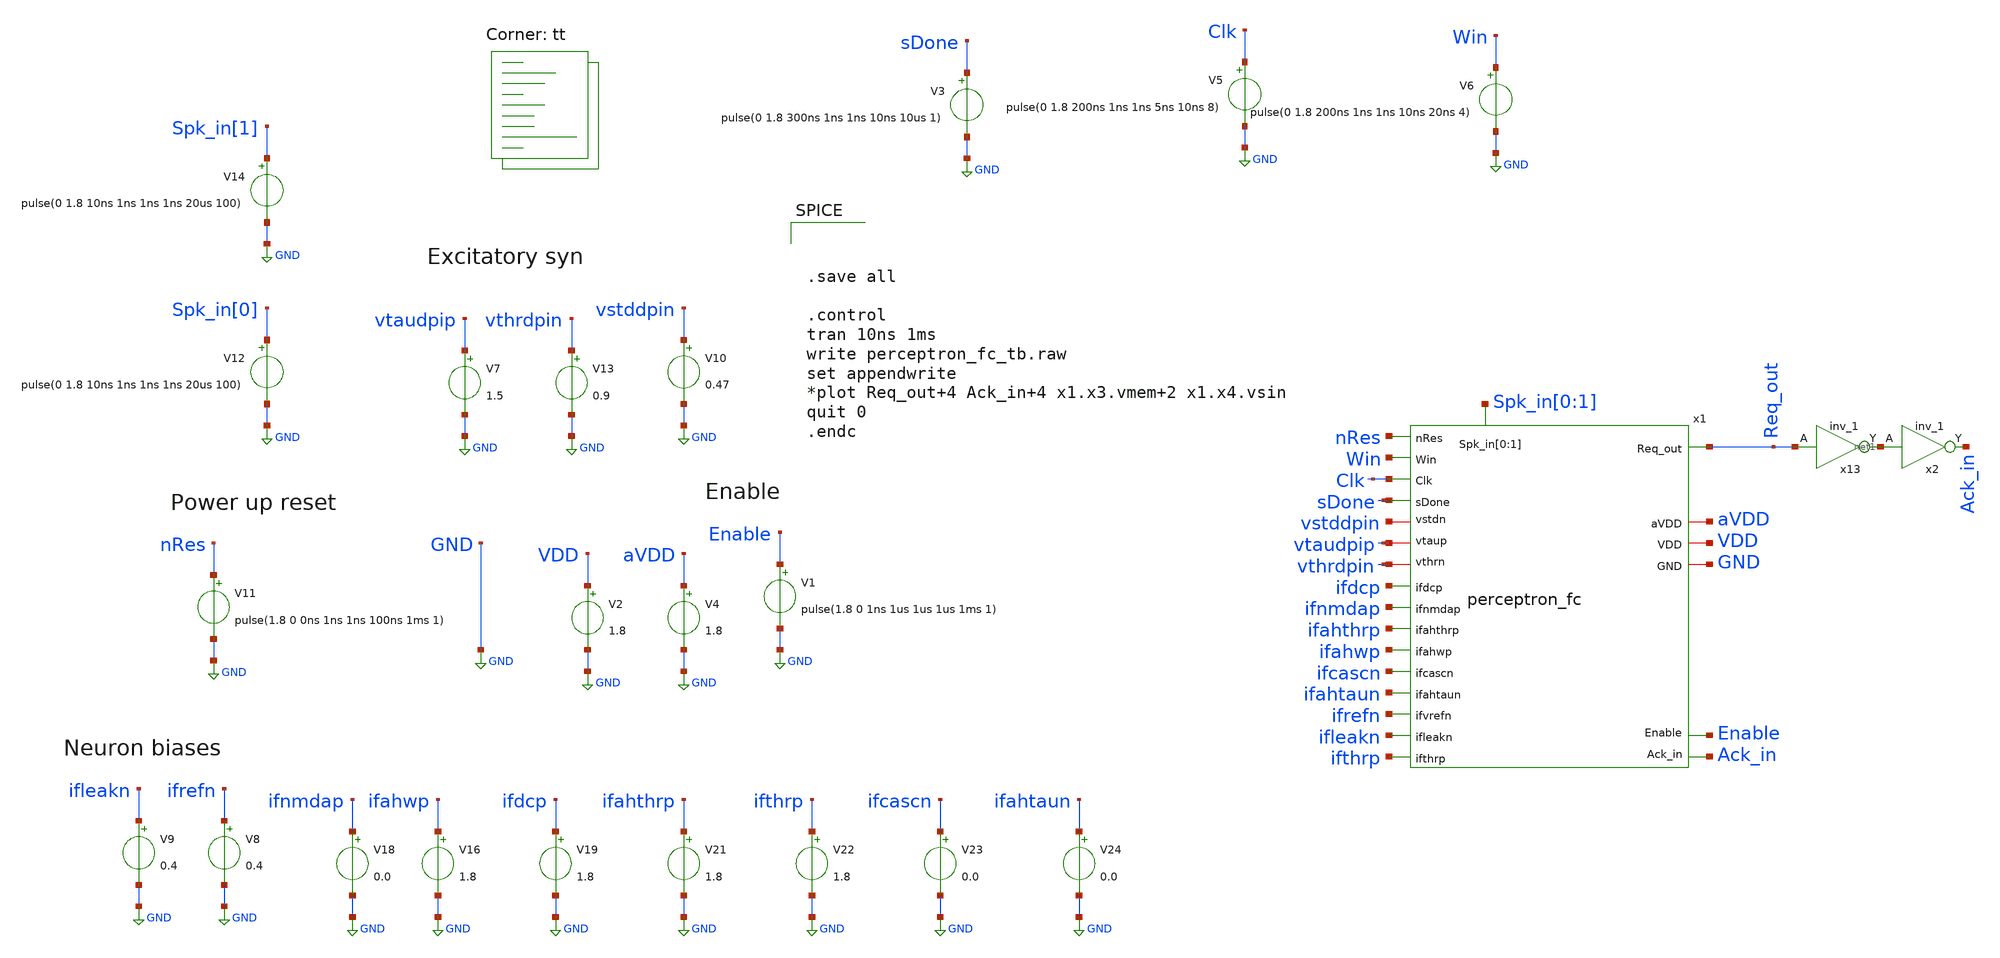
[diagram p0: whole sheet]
** sch_path: design/xschem/perceptron_fc_tb.sch
**.subckt perceptron_fc_tb
V8 ifrefn GND 0.4
V9 ifleakn GND 0.4
V16 ifahwp GND 1.8
V18 ifnmdap GND 0.0
V19 ifdcp GND 1.8
V21 ifahthrp GND 1.8
V22 ifthrp GND 1.8
V23 ifcascn GND 0.0
V24 ifahtaun GND 0.0
V2 VDD GND 1.8
V7 vtaudpip GND 1.5
V13 vthrdpin GND 0.9
V10 vstddpin GND 0.47
V12 Spk_in[0] GND pulse(0 1.8 10ns 1ns 1ns 1ns 20us 100)
V4 aVDD GND 1.8
V11 nRes GND pulse(1.8 0 0ns 1ns 1ns 100ns 1ms 1)
x13 Req_out 0 0 VDD VDD net1 sky130_fd_sc_hd__inv_1
x2 net1 0 0 VDD VDD Ack_in sky130_fd_sc_hd__inv_1
V1 Enable GND pulse(1.8 0 1ns 1us 1us 1us 1ms 1)
V3 sDone GND pulse(0 1.8 300ns 1ns 1ns 10ns 10us 1)
V5 Clk GND pulse(0 1.8 200ns 1ns 1ns 5ns 10ns 8)
V6 Win GND pulse(0 1.8 200ns 1ns 1ns 10ns 20ns 4)
x1 GND ifdcp VDD vthrdpin Win Req_out aVDD ifnmdap vtaudpip Clk ifthrp nRes vstddpin ifleakn sDone
+ Ack_in ifahthrp Enable ifahwp ifcascn Spk_in[0] Spk_in[1] ifahtaun ifrefn perceptron_fc
V14 Spk_in[1] GND pulse(0 1.8 10ns 1ns 1ns 1ns 20us 100)
**** begin user architecture code


* Standard cell simulation files
.include $::SKYWATER_STDCELLS/sky130_fd_sc_hd.spice

.lib $::SKYWATER_MODELS/sky130.lib.spice tt



.save all

.control
tran 10ns 1ms
write perceptron_fc_tb.raw
set appendwrite
*plot Req_out+4 Ack_in+4 x1.x3.vmem+2 x1.x4.vsin
quit 0
.endc


**** end user architecture code
**.ends

* expanding   symbol:  perceptron_fc.sym # of pins=23
** sym_path: design/xschem/perceptron_fc.sym
** sch_path: design/xschem/perceptron_fc.sch
.subckt perceptron_fc GND ifdcp VDD vthrn Win Req_out aVDD ifnmdap vtaup Clk ifthrp nRes vstdn
+ ifleakn sDone Ack_in ifahthrp Enable ifahwp ifcascn Spk_in[0] Spk_in[1] ifahtaun ifvrefn
*.iopin GND
*.iopin VDD
*.iopin aVDD
*.ipin Enable
*.ipin Clk
*.ipin nRes
*.ipin sDone
*.ipin Spk_in[0],Spk_in[1]
*.ipin Ack_in
*.opin Req_out
*.ipin ifdcp
*.ipin ifnmdap
*.ipin ifthrp
*.ipin ifleakn
*.ipin ifahthrp
*.ipin ifahwp
*.ipin ifcascn
*.ipin ifahtaun
*.ipin ifvrefn
*.iopin vthrn
*.iopin vtaup
*.iopin vstdn
*.ipin Win
x3 nreq_neu0 sinp0 nack_cel0 ifnmdap ifahwp ifdcp net2 ifahthrp ifthrp ifcascn ifleakn ifvrefn
+ ifahtaun GND aVDD neuron_analog_fc
x14 nRes Req_out Ack_in ack_cel0 VDD GND c_element_rj
x4 vtaup STOT vthrn Spk_in[0] vstdn GND VDD D[0] D[1] D[2] D[3] dpi_syn_exc_4bit_fc
x5 Win D[0] D[1] D[2] D[3] Dout1 Clk nRes sDone GND VDD dflip_flop_chain_4_fc
x13 ack_cel0 GND GND VDD VDD nack_cel0 sky130_fd_sc_hd__inv_1
x1 Enable sinp0 STOT GND aVDD tranmission_gate_fc
x2 Enable Req_out net1 GND aVDD tranmission_gate_fc
x7 Dout1 D[4] D[5] D[6] D[7] net3 Clk nRes sDone GND VDD dflip_flop_chain_4_fc
x6 vtaup STOT vthrn Spk_in[1] vstdn GND VDD D[4] D[5] D[6] D[7] dpi_syn_exc_4bit_fc
x9 nreq_neu0 net1 VDD GND schmitt_trigger
.ends


* expanding   symbol:  neuron_analog_fc.sym # of pins=15
** sym_path: design/xschem/neuron_analog_fc.sym
** sch_path: design/xschem/neuron_analog_fc.sch
.subckt neuron_analog_fc nreq sinp nack ifahwp ifnmdap ifahthrp vmem ifdcp ifthrp ifcascn vleakn
+ vrefn ifahtaun GND VDD
*.ipin vleakn
*.iopin GND
*.iopin VDD
*.opin nreq
*.ipin vrefn
*.ipin nack
*.ipin ifdcp
*.ipin ifthrp
*.ipin ifnmdap
*.ipin ifahwp
*.ipin ifahthrp
*.ipin ifahtaun
*.ipin ifcascn
*.iopin vmem
*.iopin sinp
XC1 GND vmem sky130_fd_pr__cap_mim_m3_1 W=11 L=11 MF=1 m=1
XM8 net4 vrefn GND GND sky130_fd_pr__nfet_01v8 L=0.25 W=0.8 nf=1 ad='int((nf+1)/2) * W/nf * 0.29' as='int((nf+2)/2) * W/nf * 0.29'
+ pd='2*int((nf+1)/2) * (W/nf + 0.29)' ps='2*int((nf+2)/2) * (W/nf + 0.29)' nrd='0.29 / W' nrs='0.29 / W'
+ sa=0 sb=0 sd=0 mult=1 m=1
XM9 net5 nack VDD VDD sky130_fd_pr__pfet_01v8 L=0.2 W=1.2 nf=1 ad='int((nf+1)/2) * W/nf * 0.29' as='int((nf+2)/2) * W/nf * 0.29'
+ pd='2*int((nf+1)/2) * (W/nf + 0.29)' ps='2*int((nf+2)/2) * (W/nf + 0.29)' nrd='0.29 / W' nrs='0.29 / W'
+ sa=0 sb=0 sd=0 mult=1 m=1
XC2 GND net3 sky130_fd_pr__cap_mim_m3_1 W=4 L=2 MF=1 m=1
XM21 vmem net3 GND GND sky130_fd_pr__nfet_01v8 L=0.25 W=1 nf=1 ad='int((nf+1)/2) * W/nf * 0.29' as='int((nf+2)/2) * W/nf * 0.29'
+ pd='2*int((nf+1)/2) * (W/nf + 0.29)' ps='2*int((nf+2)/2) * (W/nf + 0.29)' nrd='0.29 / W' nrs='0.29 / W'
+ sa=0 sb=0 sd=0 mult=1 m=1
XM15 net12 ifnmdap sinp VDD sky130_fd_pr__pfet_01v8 L=0.15 W=1 nf=1 ad='int((nf+1)/2) * W/nf * 0.29'
+ as='int((nf+2)/2) * W/nf * 0.29' pd='2*int((nf+1)/2) * (W/nf + 0.29)' ps='2*int((nf+2)/2) * (W/nf + 0.29)'
+ nrd='0.29 / W' nrs='0.29 / W' sa=0 sb=0 sd=0 mult=1 m=1
XC3 GND net8 sky130_fd_pr__cap_mim_m3_1 W=5 L=5 MF=1 m=1
XM12 GND vmem sinp VDD sky130_fd_pr__pfet_01v8 L=0.15 W=1 nf=1 ad='int((nf+1)/2) * W/nf * 0.29' as='int((nf+2)/2) * W/nf * 0.29'
+ pd='2*int((nf+1)/2) * (W/nf + 0.29)' ps='2*int((nf+2)/2) * (W/nf + 0.29)' nrd='0.29 / W' nrs='0.29 / W'
+ sa=0 sb=0 sd=0 mult=1 m=1
XM11 GND ifthrp net6 VDD sky130_fd_pr__pfet_01v8 L=0.15 W=1 nf=1 ad='int((nf+1)/2) * W/nf * 0.29' as='int((nf+2)/2) * W/nf * 0.29'
+ pd='2*int((nf+1)/2) * (W/nf + 0.29)' ps='2*int((nf+2)/2) * (W/nf + 0.29)' nrd='0.29 / W' nrs='0.29 / W'
+ sa=0 sb=0 sd=0 mult=1 m=1
XM16 net7 nack VDD VDD sky130_fd_pr__pfet_01v8 L=0.15 W=1 nf=1 ad='int((nf+1)/2) * W/nf * 0.29' as='int((nf+2)/2) * W/nf * 0.29'
+ pd='2*int((nf+1)/2) * (W/nf + 0.29)' ps='2*int((nf+2)/2) * (W/nf + 0.29)' nrd='0.29 / W' nrs='0.29 / W'
+ sa=0 sb=0 sd=0 mult=1 m=1
XM17 net9 ifahwp net7 VDD sky130_fd_pr__pfet_01v8 L=0.15 W=1 nf=1 ad='int((nf+1)/2) * W/nf * 0.29' as='int((nf+2)/2) * W/nf * 0.29'
+ pd='2*int((nf+1)/2) * (W/nf + 0.29)' ps='2*int((nf+2)/2) * (W/nf + 0.29)' nrd='0.29 / W' nrs='0.29 / W'
+ sa=0 sb=0 sd=0 mult=1 m=1
XM18 GND ifahthrp net9 VDD sky130_fd_pr__pfet_01v8 L=0.15 W=1 nf=1 ad='int((nf+1)/2) * W/nf * 0.29' as='int((nf+2)/2) * W/nf * 0.29'
+ pd='2*int((nf+1)/2) * (W/nf + 0.29)' ps='2*int((nf+2)/2) * (W/nf + 0.29)' nrd='0.29 / W' nrs='0.29 / W'
+ sa=0 sb=0 sd=0 mult=1 m=1
XM19 net8 net8 net9 VDD sky130_fd_pr__pfet_01v8 L=0.15 W=1 nf=1 ad='int((nf+1)/2) * W/nf * 0.29' as='int((nf+2)/2) * W/nf * 0.29'
+ pd='2*int((nf+1)/2) * (W/nf + 0.29)' ps='2*int((nf+2)/2) * (W/nf + 0.29)' nrd='0.29 / W' nrs='0.29 / W'
+ sa=0 sb=0 sd=0 mult=1 m=1
XM1 net11 ifdcp VDD VDD sky130_fd_pr__pfet_01v8 L=0.3 W=1 nf=1 ad='int((nf+1)/2) * W/nf * 0.29' as='int((nf+2)/2) * W/nf * 0.29'
+ pd='2*int((nf+1)/2) * (W/nf + 0.29)' ps='2*int((nf+2)/2) * (W/nf + 0.29)' nrd='0.29 / W' nrs='0.29 / W'
+ sa=0 sb=0 sd=0 mult=1 m=1
XM5 net2 nreq VDD VDD sky130_fd_pr__pfet_01v8 L=0.15 W=1 nf=1 ad='int((nf+1)/2) * W/nf * 0.29' as='int((nf+2)/2) * W/nf * 0.29'
+ pd='2*int((nf+1)/2) * (W/nf + 0.29)' ps='2*int((nf+2)/2) * (W/nf + 0.29)' nrd='0.29 / W' nrs='0.29 / W'
+ sa=0 sb=0 sd=0 mult=1 m=1
XM6 nreq vmem net2 VDD sky130_fd_pr__pfet_01v8 L=0.15 W=1 nf=1 ad='int((nf+1)/2) * W/nf * 0.29' as='int((nf+2)/2) * W/nf * 0.29'
+ pd='2*int((nf+1)/2) * (W/nf + 0.29)' ps='2*int((nf+2)/2) * (W/nf + 0.29)' nrd='0.29 / W' nrs='0.29 / W'
+ sa=0 sb=0 sd=0 mult=1 m=1
XM10 net3 nreq net5 VDD sky130_fd_pr__pfet_01v8 L=0.15 W=1 nf=1 ad='int((nf+1)/2) * W/nf * 0.29' as='int((nf+2)/2) * W/nf * 0.29'
+ pd='2*int((nf+1)/2) * (W/nf + 0.29)' ps='2*int((nf+2)/2) * (W/nf + 0.29)' nrd='0.29 / W' nrs='0.29 / W'
+ sa=0 sb=0 sd=0 mult=1 m=1
XM2 nreq vmem net1 GND sky130_fd_pr__nfet_01v8 L=0.15 W=0.65 nf=1 ad='int((nf+1)/2) * W/nf * 0.29' as='int((nf+2)/2) * W/nf * 0.29'
+ pd='2*int((nf+1)/2) * (W/nf + 0.29)' ps='2*int((nf+2)/2) * (W/nf + 0.29)' nrd='0.29 / W' nrs='0.29 / W'
+ sa=0 sb=0 sd=0 mult=1 m=1
XM3 net1 net1 GND GND sky130_fd_pr__nfet_01v8 L=0.15 W=0.65 nf=1 ad='int((nf+1)/2) * W/nf * 0.29' as='int((nf+2)/2) * W/nf * 0.29'
+ pd='2*int((nf+1)/2) * (W/nf + 0.29)' ps='2*int((nf+2)/2) * (W/nf + 0.29)' nrd='0.29 / W' nrs='0.29 / W'
+ sa=0 sb=0 sd=0 mult=1 m=1
XM7 net3 nreq net4 GND sky130_fd_pr__nfet_01v8 L=0.15 W=0.65 nf=1 ad='int((nf+1)/2) * W/nf * 0.29' as='int((nf+2)/2) * W/nf * 0.29'
+ pd='2*int((nf+1)/2) * (W/nf + 0.29)' ps='2*int((nf+2)/2) * (W/nf + 0.29)' nrd='0.29 / W' nrs='0.29 / W'
+ sa=0 sb=0 sd=0 mult=1 m=1
XM14 vmem vleakn net13 GND sky130_fd_pr__nfet_01v8 L=0.15 W=0.65 nf=1 ad='int((nf+1)/2) * W/nf * 0.29'
+ as='int((nf+2)/2) * W/nf * 0.29' pd='2*int((nf+1)/2) * (W/nf + 0.29)' ps='2*int((nf+2)/2) * (W/nf + 0.29)'
+ nrd='0.29 / W' nrs='0.29 / W' sa=0 sb=0 sd=0 mult=1 m=1
XM4 vmem nreq VDD VDD sky130_fd_pr__pfet_01v8 L=0.15 W=1 nf=1 ad='int((nf+1)/2) * W/nf * 0.29' as='int((nf+2)/2) * W/nf * 0.29'
+ pd='2*int((nf+1)/2) * (W/nf + 0.29)' ps='2*int((nf+2)/2) * (W/nf + 0.29)' nrd='0.29 / W' nrs='0.29 / W'
+ sa=0 sb=0 sd=0 mult=1 m=1
XM24 vmem vmem net6 VDD sky130_fd_pr__pfet_01v8 L=0.15 W=1 nf=1 ad='int((nf+1)/2) * W/nf * 0.29' as='int((nf+2)/2) * W/nf * 0.29'
+ pd='2*int((nf+1)/2) * (W/nf + 0.29)' ps='2*int((nf+2)/2) * (W/nf + 0.29)' nrd='0.29 / W' nrs='0.29 / W'
+ sa=0 sb=0 sd=0 mult=1 m=1
Vmeas net11 net6 0
.save i(vmeas)
Vmeas1 net13 GND 0
.save i(vmeas1)
XM13 net6 ifcascn net10 GND sky130_fd_pr__nfet_01v8 L=0.15 W=0.65 nf=1 ad='int((nf+1)/2) * W/nf * 0.29'
+ as='int((nf+2)/2) * W/nf * 0.29' pd='2*int((nf+1)/2) * (W/nf + 0.29)' ps='2*int((nf+2)/2) * (W/nf + 0.29)'
+ nrd='0.29 / W' nrs='0.29 / W' sa=0 sb=0 sd=0 mult=1 m=1
XM20 net10 net8 GND GND sky130_fd_pr__nfet_01v8 L=0.15 W=0.65 nf=1 ad='int((nf+1)/2) * W/nf * 0.29' as='int((nf+2)/2) * W/nf * 0.29'
+ pd='2*int((nf+1)/2) * (W/nf + 0.29)' ps='2*int((nf+2)/2) * (W/nf + 0.29)' nrd='0.29 / W' nrs='0.29 / W'
+ sa=0 sb=0 sd=0 mult=1 m=1
XM22 net8 ifahtaun GND GND sky130_fd_pr__nfet_01v8 L=0.15 W=0.65 nf=1 ad='int((nf+1)/2) * W/nf * 0.29'
+ as='int((nf+2)/2) * W/nf * 0.29' pd='2*int((nf+1)/2) * (W/nf + 0.29)' ps='2*int((nf+2)/2) * (W/nf + 0.29)'
+ nrd='0.29 / W' nrs='0.29 / W' sa=0 sb=0 sd=0 mult=1 m=1
.ends


* expanding   symbol:  c_element_rj.sym # of pins=6
** sym_path: design/xschem/c_element_rj.sym
** sch_path: design/xschem/c_element_rj.sch
.subckt c_element_rj nrst a b c dVDD dGND
*.iopin dGND
*.iopin dVDD
*.opin c
*.ipin b
*.ipin a
*.ipin nrst
XM14 c net6 dVDD dVDD sky130_fd_pr__pfet_01v8 L=0.15 W=1 nf=1 ad='int((nf+1)/2) * W/nf * 0.29' as='int((nf+2)/2) * W/nf * 0.29'
+ pd='2*int((nf+1)/2) * (W/nf + 0.29)' ps='2*int((nf+2)/2) * (W/nf + 0.29)' nrd='0.29 / W' nrs='0.29 / W'
+ sa=0 sb=0 sd=0 mult=1 m=1
XM5 net6 nrst dVDD dVDD sky130_fd_pr__pfet_01v8 L=0.15 W=1 nf=1 ad='int((nf+1)/2) * W/nf * 0.29' as='int((nf+2)/2) * W/nf * 0.29'
+ pd='2*int((nf+1)/2) * (W/nf + 0.29)' ps='2*int((nf+2)/2) * (W/nf + 0.29)' nrd='0.29 / W' nrs='0.29 / W'
+ sa=0 sb=0 sd=0 mult=1 m=1
XM6 net5 b dVDD dVDD sky130_fd_pr__pfet_01v8 L=0.15 W=1 nf=1 ad='int((nf+1)/2) * W/nf * 0.29' as='int((nf+2)/2) * W/nf * 0.29'
+ pd='2*int((nf+1)/2) * (W/nf + 0.29)' ps='2*int((nf+2)/2) * (W/nf + 0.29)' nrd='0.29 / W' nrs='0.29 / W'
+ sa=0 sb=0 sd=0 mult=1 m=1
XM4 net4 a dVDD dVDD sky130_fd_pr__pfet_01v8 L=0.15 W=1 nf=1 ad='int((nf+1)/2) * W/nf * 0.29' as='int((nf+2)/2) * W/nf * 0.29'
+ pd='2*int((nf+1)/2) * (W/nf + 0.29)' ps='2*int((nf+2)/2) * (W/nf + 0.29)' nrd='0.29 / W' nrs='0.29 / W'
+ sa=0 sb=0 sd=0 mult=1 m=1
XM7 net3 b net4 dVDD sky130_fd_pr__pfet_01v8 L=0.15 W=1 nf=1 ad='int((nf+1)/2) * W/nf * 0.29' as='int((nf+2)/2) * W/nf * 0.29'
+ pd='2*int((nf+1)/2) * (W/nf + 0.29)' ps='2*int((nf+2)/2) * (W/nf + 0.29)' nrd='0.29 / W' nrs='0.29 / W'
+ sa=0 sb=0 sd=0 mult=1 m=1
XM8 net3 a net5 dVDD sky130_fd_pr__pfet_01v8 L=0.15 W=1 nf=1 ad='int((nf+1)/2) * W/nf * 0.29' as='int((nf+2)/2) * W/nf * 0.29'
+ pd='2*int((nf+1)/2) * (W/nf + 0.29)' ps='2*int((nf+2)/2) * (W/nf + 0.29)' nrd='0.29 / W' nrs='0.29 / W'
+ sa=0 sb=0 sd=0 mult=1 m=1
XM10 net5 c net4 dVDD sky130_fd_pr__pfet_01v8 L=0.15 W=1 nf=1 ad='int((nf+1)/2) * W/nf * 0.29' as='int((nf+2)/2) * W/nf * 0.29'
+ pd='2*int((nf+1)/2) * (W/nf + 0.29)' ps='2*int((nf+2)/2) * (W/nf + 0.29)' nrd='0.29 / W' nrs='0.29 / W'
+ sa=0 sb=0 sd=0 mult=1 m=1
XM12 c net6 dGND dGND sky130_fd_pr__nfet_01v8 L=0.15 W=0.65 nf=1 ad='int((nf+1)/2) * W/nf * 0.29' as='int((nf+2)/2) * W/nf * 0.29'
+ pd='2*int((nf+1)/2) * (W/nf + 0.29)' ps='2*int((nf+2)/2) * (W/nf + 0.29)' nrd='0.29 / W' nrs='0.29 / W'
+ sa=0 sb=0 sd=0 mult=1 m=1
XM1 net3 nrst net6 dGND sky130_fd_pr__nfet_01v8 L=0.15 W=0.65 nf=1 ad='int((nf+1)/2) * W/nf * 0.29' as='int((nf+2)/2) * W/nf * 0.29'
+ pd='2*int((nf+1)/2) * (W/nf + 0.29)' ps='2*int((nf+2)/2) * (W/nf + 0.29)' nrd='0.29 / W' nrs='0.29 / W'
+ sa=0 sb=0 sd=0 mult=1 m=1
XM2 net3 b net1 dGND sky130_fd_pr__nfet_01v8 L=0.15 W=0.65 nf=1 ad='int((nf+1)/2) * W/nf * 0.29' as='int((nf+2)/2) * W/nf * 0.29'
+ pd='2*int((nf+1)/2) * (W/nf + 0.29)' ps='2*int((nf+2)/2) * (W/nf + 0.29)' nrd='0.29 / W' nrs='0.29 / W'
+ sa=0 sb=0 sd=0 mult=1 m=1
XM3 net3 a net2 dGND sky130_fd_pr__nfet_01v8 L=0.15 W=0.65 nf=1 ad='int((nf+1)/2) * W/nf * 0.29' as='int((nf+2)/2) * W/nf * 0.29'
+ pd='2*int((nf+1)/2) * (W/nf + 0.29)' ps='2*int((nf+2)/2) * (W/nf + 0.29)' nrd='0.29 / W' nrs='0.29 / W'
+ sa=0 sb=0 sd=0 mult=1 m=1
XM9 net2 c net1 dGND sky130_fd_pr__nfet_01v8 L=0.15 W=0.65 nf=1 ad='int((nf+1)/2) * W/nf * 0.29' as='int((nf+2)/2) * W/nf * 0.29'
+ pd='2*int((nf+1)/2) * (W/nf + 0.29)' ps='2*int((nf+2)/2) * (W/nf + 0.29)' nrd='0.29 / W' nrs='0.29 / W'
+ sa=0 sb=0 sd=0 mult=1 m=1
XM11 net1 a dGND dGND sky130_fd_pr__nfet_01v8 L=0.15 W=0.65 nf=1 ad='int((nf+1)/2) * W/nf * 0.29' as='int((nf+2)/2) * W/nf * 0.29'
+ pd='2*int((nf+1)/2) * (W/nf + 0.29)' ps='2*int((nf+2)/2) * (W/nf + 0.29)' nrd='0.29 / W' nrs='0.29 / W'
+ sa=0 sb=0 sd=0 mult=1 m=1
XM13 net2 b dGND dGND sky130_fd_pr__nfet_01v8 L=0.15 W=0.65 nf=1 ad='int((nf+1)/2) * W/nf * 0.29' as='int((nf+2)/2) * W/nf * 0.29'
+ pd='2*int((nf+1)/2) * (W/nf + 0.29)' ps='2*int((nf+2)/2) * (W/nf + 0.29)' nrd='0.29 / W' nrs='0.29 / W'
+ sa=0 sb=0 sd=0 mult=1 m=1
.ends


* expanding   symbol:  dpi_syn_exc_4bit_fc.sym # of pins=8
** sym_path: design/xschem/dpi_syn_exc_4bit_fc.sym
** sch_path: design/xschem/dpi_syn_exc_4bit_fc.sch
.subckt dpi_syn_exc_4bit_fc vtau sout vthn spk vstdn GND VDD weight[0] weight[1] weight[2] weight[3]
*.iopin GND
*.iopin VDD
*.iopin vtau
*.iopin vstdn
*.ipin spk
*.opin sout
*.iopin vthn
*.ipin weight[0],weight[1],weight[2],weight[3]
XM2 net3 spk net1 GND sky130_fd_pr__nfet_01v8 L=0.25 W=0.8 nf=1 ad='int((nf+1)/2) * W/nf * 0.29' as='int((nf+2)/2) * W/nf * 0.29'
+ pd='2*int((nf+1)/2) * (W/nf + 0.29)' ps='2*int((nf+2)/2) * (W/nf + 0.29)' nrd='0.29 / W' nrs='0.29 / W'
+ sa=0 sb=0 sd=0 mult=1 m=1
XC1 vsin VDD sky130_fd_pr__cap_mim_m3_1 W=5 L=5 MF=1 m=1
XM5 vsin vtau VDD VDD sky130_fd_pr__pfet_01v8 L=0.2 W=1.2 nf=1 ad='int((nf+1)/2) * W/nf * 0.29' as='int((nf+2)/2) * W/nf * 0.29'
+ pd='2*int((nf+1)/2) * (W/nf + 0.29)' ps='2*int((nf+2)/2) * (W/nf + 0.29)' nrd='0.29 / W' nrs='0.29 / W'
+ sa=0 sb=0 sd=0 mult=1 m=1
XM6 sout vsin VDD VDD sky130_fd_pr__pfet_01v8 L=0.2 W=1.2 nf=1 ad='int((nf+1)/2) * W/nf * 0.29' as='int((nf+2)/2) * W/nf * 0.29'
+ pd='2*int((nf+1)/2) * (W/nf + 0.29)' ps='2*int((nf+2)/2) * (W/nf + 0.29)' nrd='0.29 / W' nrs='0.29 / W'
+ sa=0 sb=0 sd=0 mult=1 m=1
XM1 net1 vstdn net2 GND sky130_fd_pr__nfet_01v8 L=0.5 W=0.8 nf=1 ad='int((nf+1)/2) * W/nf * 0.29' as='int((nf+2)/2) * W/nf * 0.29'
+ pd='2*int((nf+1)/2) * (W/nf + 0.29)' ps='2*int((nf+2)/2) * (W/nf + 0.29)' nrd='0.29 / W' nrs='0.29 / W'
+ sa=0 sb=0 sd=0 mult=1 m=1
XM4 vsin vsin net3 GND sky130_fd_pr__nfet_01v8 L=0.25 W=0.8 nf=1 ad='int((nf+1)/2) * W/nf * 0.29' as='int((nf+2)/2) * W/nf * 0.29'
+ pd='2*int((nf+1)/2) * (W/nf + 0.29)' ps='2*int((nf+2)/2) * (W/nf + 0.29)' nrd='0.29 / W' nrs='0.29 / W'
+ sa=0 sb=0 sd=0 mult=1 m=1
XM3 VDD vthn net3 GND sky130_fd_pr__nfet_01v8 L=0.25 W=0.8 nf=1 ad='int((nf+1)/2) * W/nf * 0.29' as='int((nf+2)/2) * W/nf * 0.29'
+ pd='2*int((nf+1)/2) * (W/nf + 0.29)' ps='2*int((nf+2)/2) * (W/nf + 0.29)' nrd='0.29 / W' nrs='0.29 / W'
+ sa=0 sb=0 sd=0 mult=1 m=1
XM7 net1 vstdn net4 GND sky130_fd_pr__nfet_01v8 L=2.0 W=0.8 nf=1 ad='int((nf+1)/2) * W/nf * 0.29' as='int((nf+2)/2) * W/nf * 0.29'
+ pd='2*int((nf+1)/2) * (W/nf + 0.29)' ps='2*int((nf+2)/2) * (W/nf + 0.29)' nrd='0.29 / W' nrs='0.29 / W'
+ sa=0 sb=0 sd=0 mult=1 m=1
XM8 net1 vstdn net5 GND sky130_fd_pr__nfet_01v8 L=4.0 W=0.8 nf=1 ad='int((nf+1)/2) * W/nf * 0.29' as='int((nf+2)/2) * W/nf * 0.29'
+ pd='2*int((nf+1)/2) * (W/nf + 0.29)' ps='2*int((nf+2)/2) * (W/nf + 0.29)' nrd='0.29 / W' nrs='0.29 / W'
+ sa=0 sb=0 sd=0 mult=1 m=1
XM9 net1 vstdn net6 GND sky130_fd_pr__nfet_01v8 L=8.0 W=0.8 nf=1 ad='int((nf+1)/2) * W/nf * 0.29' as='int((nf+2)/2) * W/nf * 0.29'
+ pd='2*int((nf+1)/2) * (W/nf + 0.29)' ps='2*int((nf+2)/2) * (W/nf + 0.29)' nrd='0.29 / W' nrs='0.29 / W'
+ sa=0 sb=0 sd=0 mult=1 m=1
XM10 net2 weight[0] GND GND sky130_fd_pr__nfet_01v8 L=0.25 W=0.8 nf=1 ad='int((nf+1)/2) * W/nf * 0.29'
+ as='int((nf+2)/2) * W/nf * 0.29' pd='2*int((nf+1)/2) * (W/nf + 0.29)' ps='2*int((nf+2)/2) * (W/nf + 0.29)'
+ nrd='0.29 / W' nrs='0.29 / W' sa=0 sb=0 sd=0 mult=1 m=1
XM11 net4 weight[1] GND GND sky130_fd_pr__nfet_01v8 L=0.25 W=0.8 nf=1 ad='int((nf+1)/2) * W/nf * 0.29'
+ as='int((nf+2)/2) * W/nf * 0.29' pd='2*int((nf+1)/2) * (W/nf + 0.29)' ps='2*int((nf+2)/2) * (W/nf + 0.29)'
+ nrd='0.29 / W' nrs='0.29 / W' sa=0 sb=0 sd=0 mult=1 m=1
XM12 net5 weight[2] GND GND sky130_fd_pr__nfet_01v8 L=0.25 W=0.8 nf=1 ad='int((nf+1)/2) * W/nf * 0.29'
+ as='int((nf+2)/2) * W/nf * 0.29' pd='2*int((nf+1)/2) * (W/nf + 0.29)' ps='2*int((nf+2)/2) * (W/nf + 0.29)'
+ nrd='0.29 / W' nrs='0.29 / W' sa=0 sb=0 sd=0 mult=1 m=1
XM13 net6 weight[3] GND GND sky130_fd_pr__nfet_01v8 L=0.25 W=0.8 nf=1 ad='int((nf+1)/2) * W/nf * 0.29'
+ as='int((nf+2)/2) * W/nf * 0.29' pd='2*int((nf+1)/2) * (W/nf + 0.29)' ps='2*int((nf+2)/2) * (W/nf + 0.29)'
+ nrd='0.29 / W' nrs='0.29 / W' sa=0 sb=0 sd=0 mult=1 m=1
.ends


* expanding   symbol:  dflip_flop_chain_4_fc.sym # of pins=8
** sym_path: design/xschem/dflip_flop_chain_4_fc.sym
** sch_path: design/xschem/dflip_flop_chain_4_fc.sch
.subckt dflip_flop_chain_4_fc Da D[0] D[1] D[2] D[3] Dout CLK nRes sDone VDD GND
*.ipin Da
*.opin D[0],D[1],D[2],D[3]
*.ipin CLK
*.ipin nRes
*.ipin sDone
*.opin Dout
*.iopin VDD
*.iopin GND
x1[0] CLK Da nRes GND GND VDD VDD D_internal[0] sky130_fd_sc_hd__dfrtp_1
x1[1] CLK D_internal[0] nRes GND GND VDD VDD D_internal[1] sky130_fd_sc_hd__dfrtp_1
x1[2] CLK D_internal[1] nRes GND GND VDD VDD D_internal[2] sky130_fd_sc_hd__dfrtp_1
x1[3] CLK D_internal[2] nRes GND GND VDD VDD Dout sky130_fd_sc_hd__dfrtp_1
x2[0] D_internal[0] sDone nRes GND GND VDD VDD D[0] sky130_fd_sc_hd__dlrtp_1
x2[1] D_internal[1] sDone nRes GND GND VDD VDD D[1] sky130_fd_sc_hd__dlrtp_1
x2[2] D_internal[2] sDone nRes GND GND VDD VDD D[2] sky130_fd_sc_hd__dlrtp_1
x2[3] Dout sDone nRes GND GND VDD VDD D[3] sky130_fd_sc_hd__dlrtp_1
.ends


* expanding   symbol:  tranmission_gate_fc.sym # of pins=5
** sym_path: design/xschem/tranmission_gate_fc.sym
** sch_path: design/xschem/tranmission_gate_fc.sch
.subckt tranmission_gate_fc ST OUT IN GND VDD
*.iopin GND
*.iopin VDD
*.ipin ST
*.ipin IN
*.opin OUT
x13 ST GND GND VDD VDD net1 sky130_fd_sc_hd__inv_1
XM19 IN net1 OUT VDD sky130_fd_pr__pfet_01v8 L=0.15 W=1 nf=1 ad='int((nf+1)/2) * W/nf * 0.29' as='int((nf+2)/2) * W/nf * 0.29'
+ pd='2*int((nf+1)/2) * (W/nf + 0.29)' ps='2*int((nf+2)/2) * (W/nf + 0.29)' nrd='0.29 / W' nrs='0.29 / W'
+ sa=0 sb=0 sd=0 mult=1 m=1
XM2 IN ST OUT GND sky130_fd_pr__nfet_01v8 L=0.15 W=0.65 nf=1 ad='int((nf+1)/2) * W/nf * 0.29' as='int((nf+2)/2) * W/nf * 0.29'
+ pd='2*int((nf+1)/2) * (W/nf + 0.29)' ps='2*int((nf+2)/2) * (W/nf + 0.29)' nrd='0.29 / W' nrs='0.29 / W'
+ sa=0 sb=0 sd=0 mult=1 m=1
.ends


* expanding   symbol:  schmitt_trigger.sym # of pins=4
** sym_path: design/xschem/schmitt_trigger.sym
** sch_path: design/xschem/schmitt_trigger.sch
.subckt schmitt_trigger A Y VDD GND
*.ipin A
*.opin Y
*.iopin VDD
*.iopin GND
XM3 net2 A GND GND sky130_fd_pr__nfet_01v8 L=0.15 W=0.65 nf=1 ad='int((nf+1)/2) * W/nf * 0.29' as='int((nf+2)/2) * W/nf * 0.29'
+ pd='2*int((nf+1)/2) * (W/nf + 0.29)' ps='2*int((nf+2)/2) * (W/nf + 0.29)' nrd='0.29 / W' nrs='0.29 / W'
+ sa=0 sb=0 sd=0 mult=1 m=1
XM1 Y A net2 GND sky130_fd_pr__nfet_01v8 L=0.15 W=0.65 nf=1 ad='int((nf+1)/2) * W/nf * 0.29' as='int((nf+2)/2) * W/nf * 0.29'
+ pd='2*int((nf+1)/2) * (W/nf + 0.29)' ps='2*int((nf+2)/2) * (W/nf + 0.29)' nrd='0.29 / W' nrs='0.29 / W'
+ sa=0 sb=0 sd=0 mult=1 m=1
XM7 VDD Y net2 GND sky130_fd_pr__nfet_01v8 L=0.15 W=0.42 nf=1 ad='int((nf+1)/2) * W/nf * 0.29' as='int((nf+2)/2) * W/nf * 0.29'
+ pd='2*int((nf+1)/2) * (W/nf + 0.29)' ps='2*int((nf+2)/2) * (W/nf + 0.29)' nrd='0.29 / W' nrs='0.29 / W'
+ sa=0 sb=0 sd=0 mult=1 m=1
XM4 net1 A VDD VDD sky130_fd_pr__pfet_01v8 L=0.15 W=1 nf=1 ad='int((nf+1)/2) * W/nf * 0.29' as='int((nf+2)/2) * W/nf * 0.29'
+ pd='2*int((nf+1)/2) * (W/nf + 0.29)' ps='2*int((nf+2)/2) * (W/nf + 0.29)' nrd='0.29 / W' nrs='0.29 / W'
+ sa=0 sb=0 sd=0 mult=1 m=1
XM2 Y A net1 VDD sky130_fd_pr__pfet_01v8 L=0.15 W=1 nf=1 ad='int((nf+1)/2) * W/nf * 0.29' as='int((nf+2)/2) * W/nf * 0.29'
+ pd='2*int((nf+1)/2) * (W/nf + 0.29)' ps='2*int((nf+2)/2) * (W/nf + 0.29)' nrd='0.29 / W' nrs='0.29 / W'
+ sa=0 sb=0 sd=0 mult=1 m=1
XM5 GND Y net1 VDD sky130_fd_pr__pfet_01v8 L=0.15 W=0.82 nf=1 ad='int((nf+1)/2) * W/nf * 0.29' as='int((nf+2)/2) * W/nf * 0.29'
+ pd='2*int((nf+1)/2) * (W/nf + 0.29)' ps='2*int((nf+2)/2) * (W/nf + 0.29)' nrd='0.29 / W' nrs='0.29 / W'
+ sa=0 sb=0 sd=0 mult=1 m=1
.ends

.GLOBAL GND
.end
